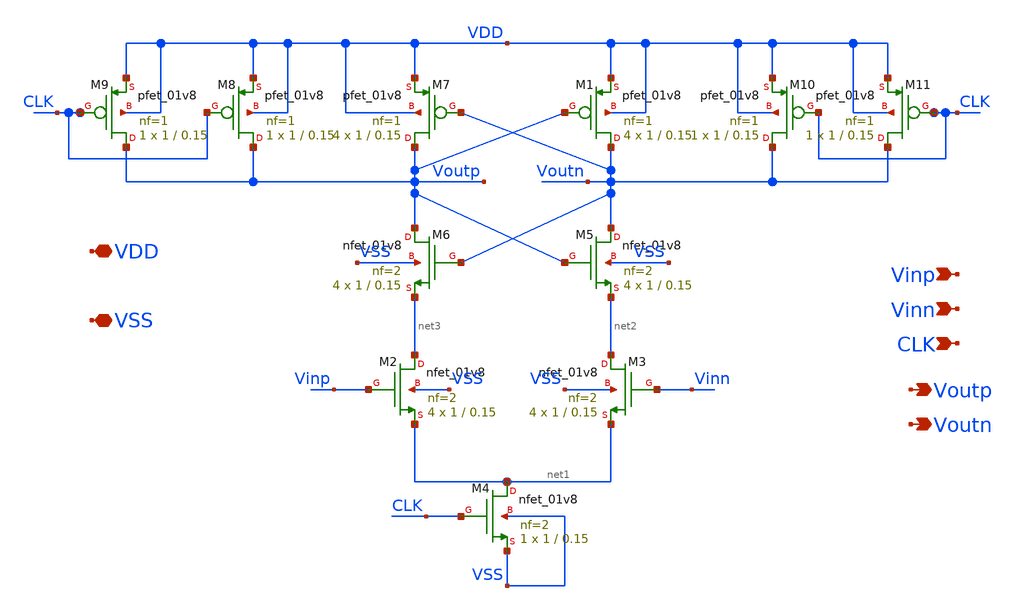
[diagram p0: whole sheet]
** sch_path: xschem/Comparator.sch
**.subckt Comparator VDD VSS Vinp Vinn CLK Voutp Voutn
*.iopin VDD
*.iopin VSS
*.ipin Vinp
*.ipin Vinn
*.ipin CLK
*.opin Voutp
*.opin Voutn
XM1 Voutn Voutp VDD VDD sky130_fd_pr__pfet_01v8 L=0.15 W=1 nf=1 ad='int((nf+1)/2) * W/nf * 0.29' as='int((nf+2)/2) * W/nf * 0.29'
+ pd='2*int((nf+1)/2) * (W/nf + 0.29)' ps='2*int((nf+2)/2) * (W/nf + 0.29)' nrd='0.29 / W' nrs='0.29 / W'
+ sa=0 sb=0 sd=0 mult=4 m=4
XM2 net3 Vinp net1 VSS sky130_fd_pr__nfet_01v8 L=0.15 W=1 nf=2 ad='int((nf+1)/2) * W/nf * 0.29' as='int((nf+2)/2) * W/nf * 0.29'
+ pd='2*int((nf+1)/2) * (W/nf + 0.29)' ps='2*int((nf+2)/2) * (W/nf + 0.29)' nrd='0.29 / W' nrs='0.29 / W'
+ sa=0 sb=0 sd=0 mult=4 m=4
XM3 net2 Vinn net1 VSS sky130_fd_pr__nfet_01v8 L=0.15 W=1 nf=2 ad='int((nf+1)/2) * W/nf * 0.29' as='int((nf+2)/2) * W/nf * 0.29'
+ pd='2*int((nf+1)/2) * (W/nf + 0.29)' ps='2*int((nf+2)/2) * (W/nf + 0.29)' nrd='0.29 / W' nrs='0.29 / W'
+ sa=0 sb=0 sd=0 mult=4 m=4
XM4 net1 CLK VSS VSS sky130_fd_pr__nfet_01v8 L=0.15 W=1 nf=2 ad='int((nf+1)/2) * W/nf * 0.29' as='int((nf+2)/2) * W/nf * 0.29'
+ pd='2*int((nf+1)/2) * (W/nf + 0.29)' ps='2*int((nf+2)/2) * (W/nf + 0.29)' nrd='0.29 / W' nrs='0.29 / W'
+ sa=0 sb=0 sd=0 mult=1 m=1
XM5 Voutn Voutp net2 VSS sky130_fd_pr__nfet_01v8 L=0.15 W=1 nf=2 ad='int((nf+1)/2) * W/nf * 0.29' as='int((nf+2)/2) * W/nf * 0.29'
+ pd='2*int((nf+1)/2) * (W/nf + 0.29)' ps='2*int((nf+2)/2) * (W/nf + 0.29)' nrd='0.29 / W' nrs='0.29 / W'
+ sa=0 sb=0 sd=0 mult=4 m=4
XM6 Voutp Voutn net3 VSS sky130_fd_pr__nfet_01v8 L=0.15 W=1 nf=2 ad='int((nf+1)/2) * W/nf * 0.29' as='int((nf+2)/2) * W/nf * 0.29'
+ pd='2*int((nf+1)/2) * (W/nf + 0.29)' ps='2*int((nf+2)/2) * (W/nf + 0.29)' nrd='0.29 / W' nrs='0.29 / W'
+ sa=0 sb=0 sd=0 mult=4 m=4
XM7 Voutp Voutn VDD VDD sky130_fd_pr__pfet_01v8 L=0.15 W=1 nf=1 ad='int((nf+1)/2) * W/nf * 0.29' as='int((nf+2)/2) * W/nf * 0.29'
+ pd='2*int((nf+1)/2) * (W/nf + 0.29)' ps='2*int((nf+2)/2) * (W/nf + 0.29)' nrd='0.29 / W' nrs='0.29 / W'
+ sa=0 sb=0 sd=0 mult=4 m=4
XM8 Voutp CLK VDD VDD sky130_fd_pr__pfet_01v8 L=0.15 W=1 nf=1 ad='int((nf+1)/2) * W/nf * 0.29' as='int((nf+2)/2) * W/nf * 0.29'
+ pd='2*int((nf+1)/2) * (W/nf + 0.29)' ps='2*int((nf+2)/2) * (W/nf + 0.29)' nrd='0.29 / W' nrs='0.29 / W'
+ sa=0 sb=0 sd=0 mult=1 m=1
XM9 Voutp CLK VDD VDD sky130_fd_pr__pfet_01v8 L=0.15 W=1 nf=1 ad='int((nf+1)/2) * W/nf * 0.29' as='int((nf+2)/2) * W/nf * 0.29'
+ pd='2*int((nf+1)/2) * (W/nf + 0.29)' ps='2*int((nf+2)/2) * (W/nf + 0.29)' nrd='0.29 / W' nrs='0.29 / W'
+ sa=0 sb=0 sd=0 mult=1 m=1
XM10 Voutn CLK VDD VDD sky130_fd_pr__pfet_01v8 L=0.15 W=1 nf=1 ad='int((nf+1)/2) * W/nf * 0.29' as='int((nf+2)/2) * W/nf * 0.29'
+ pd='2*int((nf+1)/2) * (W/nf + 0.29)' ps='2*int((nf+2)/2) * (W/nf + 0.29)' nrd='0.29 / W' nrs='0.29 / W'
+ sa=0 sb=0 sd=0 mult=1 m=1
XM11 Voutn CLK VDD VDD sky130_fd_pr__pfet_01v8 L=0.15 W=1 nf=1 ad='int((nf+1)/2) * W/nf * 0.29' as='int((nf+2)/2) * W/nf * 0.29'
+ pd='2*int((nf+1)/2) * (W/nf + 0.29)' ps='2*int((nf+2)/2) * (W/nf + 0.29)' nrd='0.29 / W' nrs='0.29 / W'
+ sa=0 sb=0 sd=0 mult=1 m=1
**.ends
.end
